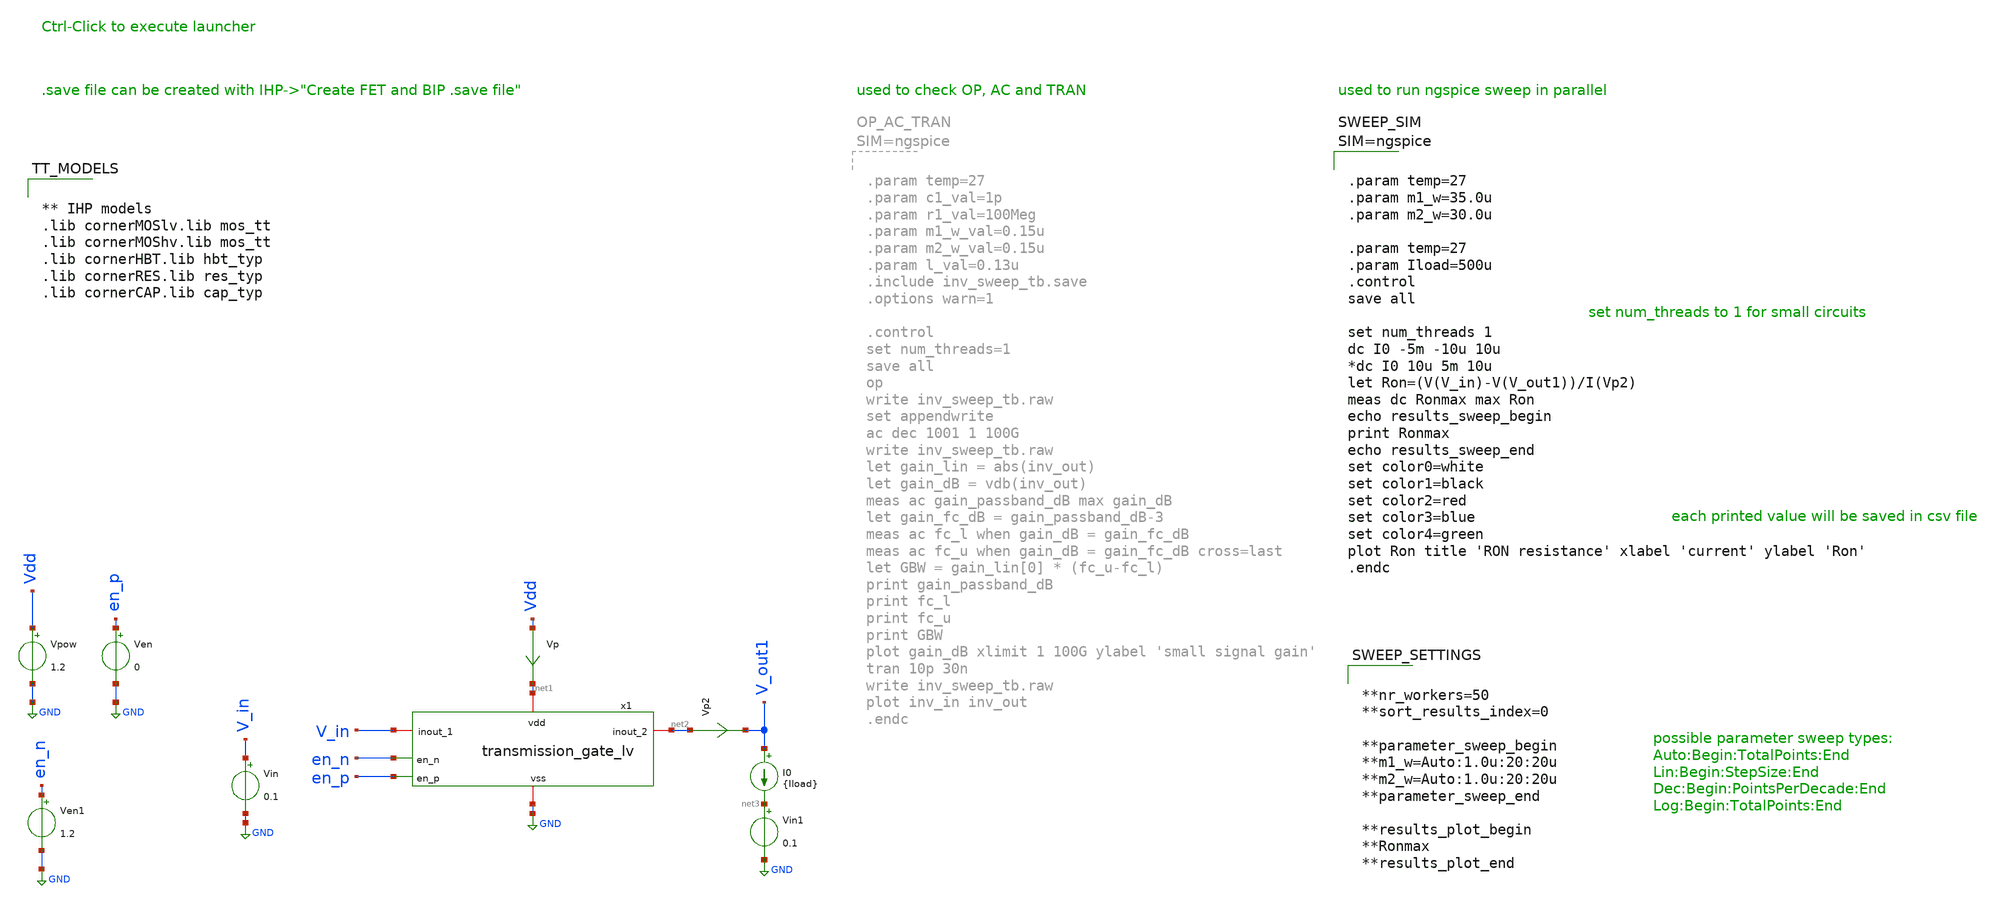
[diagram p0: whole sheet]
** sch_path: design_data/xschem/tgate_sweep_tb.sch
**.subckt tgate_sweep_tb
Vpow Vdd GND 1.2
Vp Vdd net1 0
.save i(vp)
Vin V_in GND 0.1
Ven en_p GND 0
Ven1 en_n GND 1.2
I0 V_out1 net3 {Iload}
Vp2 net2 V_out1 0
.save i(vp2)
Vin1 net3 GND 0.1
x1 net1 en_n V_in net2 en_p GND transmission_gate_lv
**** begin user architecture code


** IHP models
.lib cornerMOSlv.lib mos_tt
.lib cornerMOShv.lib mos_tt
.lib cornerHBT.lib hbt_typ
.lib cornerRES.lib res_typ
.lib cornerCAP.lib cap_typ





.param temp=27
.param m1_w=35.0u
.param m2_w=30.0u

.param temp=27
.param Iload=500u
.control
save all

set num_threads 1
dc I0 -5m -10u 10u
*dc I0 10u 5m 10u
let Ron=(V(V_in)-V(V_out1))/I(Vp2)
meas dc Ronmax max Ron
echo results_sweep_begin
print Ronmax
echo results_sweep_end
set color0=white
set color1=black
set color2=red
set color3=blue
set color4=green
plot Ron title 'RON resistance' xlabel 'current' ylabel 'Ron'
.endc





**nr_workers=50
**sort_results_index=0

**parameter_sweep_begin
**m1_w=Auto:1.0u:20:20u
**m2_w=Auto:1.0u:20:20u
**parameter_sweep_end

**results_plot_begin
**Ronmax
**results_plot_end


**** end user architecture code
**.ends

* expanding   symbol:  transmission_gate_lv.sym # of pins=6
** sym_path: design_data/xschem/transmission_gate_lv.sym
** sch_path: design_data/xschem/transmission_gate_lv.sch
.subckt transmission_gate_lv vdd en_n inout_1 inout_2 en_p vss
*.iopin inout_1
*.iopin inout_2
*.ipin en_p
*.iopin vdd
*.iopin vss
*.ipin en_n
XR1 vss net1 ptap1 R=1.903 w=20.78e-6 l=20.78e-6
XR2 vdd net2 ntap1 R=1.903 w=20.78e-6 l=20.78e-6
XM2 inout_2 en_n inout_1 net2 sg13_lv_pmos w={m2_w} l=0.13u ng=10 m=1 mm_ok=1
XM1 inout_1 en_p inout_2 net1 sg13_lv_nmos w={m1_w} l=0.13u ng=10 m=1 mm_ok=1
.ends

.GLOBAL GND
.end
